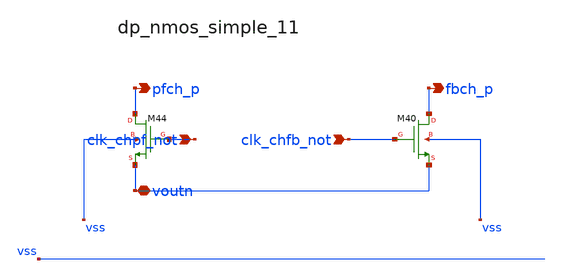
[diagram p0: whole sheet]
** sch_path: analog-db/raw/ia_003_fan_chopper_pf/hier/blocks/dp_nmos_simple_11.sch
**.subckt dp_nmos_simple_11 clk_chpf_not clk_chfb_not voutn pfch_p fbch_p
*.ipin clk_chpf_not
*.ipin clk_chfb_not
*.iopin voutn
*.opin pfch_p
*.opin fbch_p
XM40 fbch_p clk_chfb_not voutn vss sg13_lv_nmos w=x_dut_xm40_w l=x_dut_xm40_l ng=1 m=x_dut_xm40_m
XM44 pfch_p clk_chpf_not voutn vss sg13_lv_nmos w=x_dut_xm44_w l=x_dut_xm44_l ng=1 m=x_dut_xm44_m
**.ends
.end
